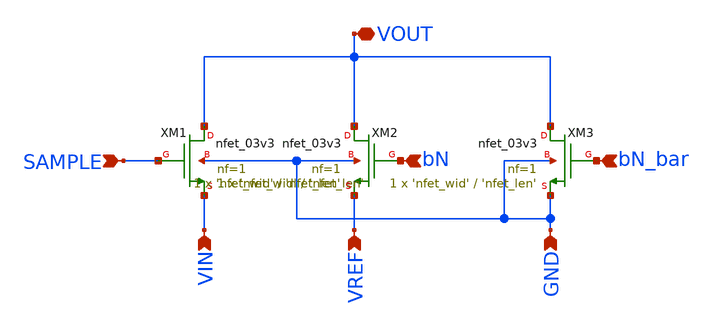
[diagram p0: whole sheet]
** sch_path: dac/schematic/unit_switch.sch
**.subckt unit_switch GND VREF VIN SAMPLE VOUT bN bN_bar
*.ipin GND
*.ipin VREF
*.ipin VIN
*.ipin SAMPLE
*.iopin VOUT
*.ipin bN
*.ipin bN_bar
XM1 VOUT SAMPLE VIN GND nfet_03v3 L='nfet_len' W='nfet_wid' nf=1 ad='int((nf+1)/2) * W/nf * 0.18u' as='int((nf+2)/2) * W/nf * 0.18u'
+ pd='2*int((nf+1)/2) * (W/nf + 0.18u)' ps='2*int((nf+2)/2) * (W/nf + 0.18u)' nrd='0.18u / W' nrs='0.18u / W'
+ sa=0 sb=0 sd=0 m=1
XM2 VOUT bN VREF GND nfet_03v3 L='nfet_len' W='nfet_wid' nf=1 ad='int((nf+1)/2) * W/nf * 0.18u' as='int((nf+2)/2) * W/nf * 0.18u'
+ pd='2*int((nf+1)/2) * (W/nf + 0.18u)' ps='2*int((nf+2)/2) * (W/nf + 0.18u)' nrd='0.18u / W' nrs='0.18u / W'
+ sa=0 sb=0 sd=0 m=1
XM3 VOUT bN_bar GND GND nfet_03v3 L='nfet_len' W='nfet_wid' nf=1 ad='int((nf+1)/2) * W/nf * 0.18u' as='int((nf+2)/2) * W/nf * 0.18u'
+ pd='2*int((nf+1)/2) * (W/nf + 0.18u)' ps='2*int((nf+2)/2) * (W/nf + 0.18u)' nrd='0.18u / W' nrs='0.18u / W'
+ sa=0 sb=0 sd=0 m=1
**.ends
.end
